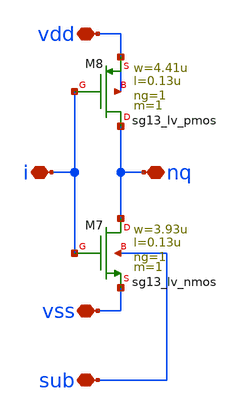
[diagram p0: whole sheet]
** sch_path: ihp-sg13cmos5l/libs.tech/xschem/hm_stdcells/sg13g2_io_inv_x1_noptap.sch
**.subckt sg13g2_io_inv_x1_noptap vss nq i vdd sub
*.iopin vss
*.iopin nq
*.iopin i
*.iopin vdd
*.iopin sub
XM7 nq i vss sub sg13_lv_nmos w=3.93u l=0.13u ng=1 m=1 mm_ok=1
XM8 nq i vdd vdd sg13_lv_pmos w=4.41u l=0.13u ng=1 m=1 mm_ok=1
**.ends
.end
